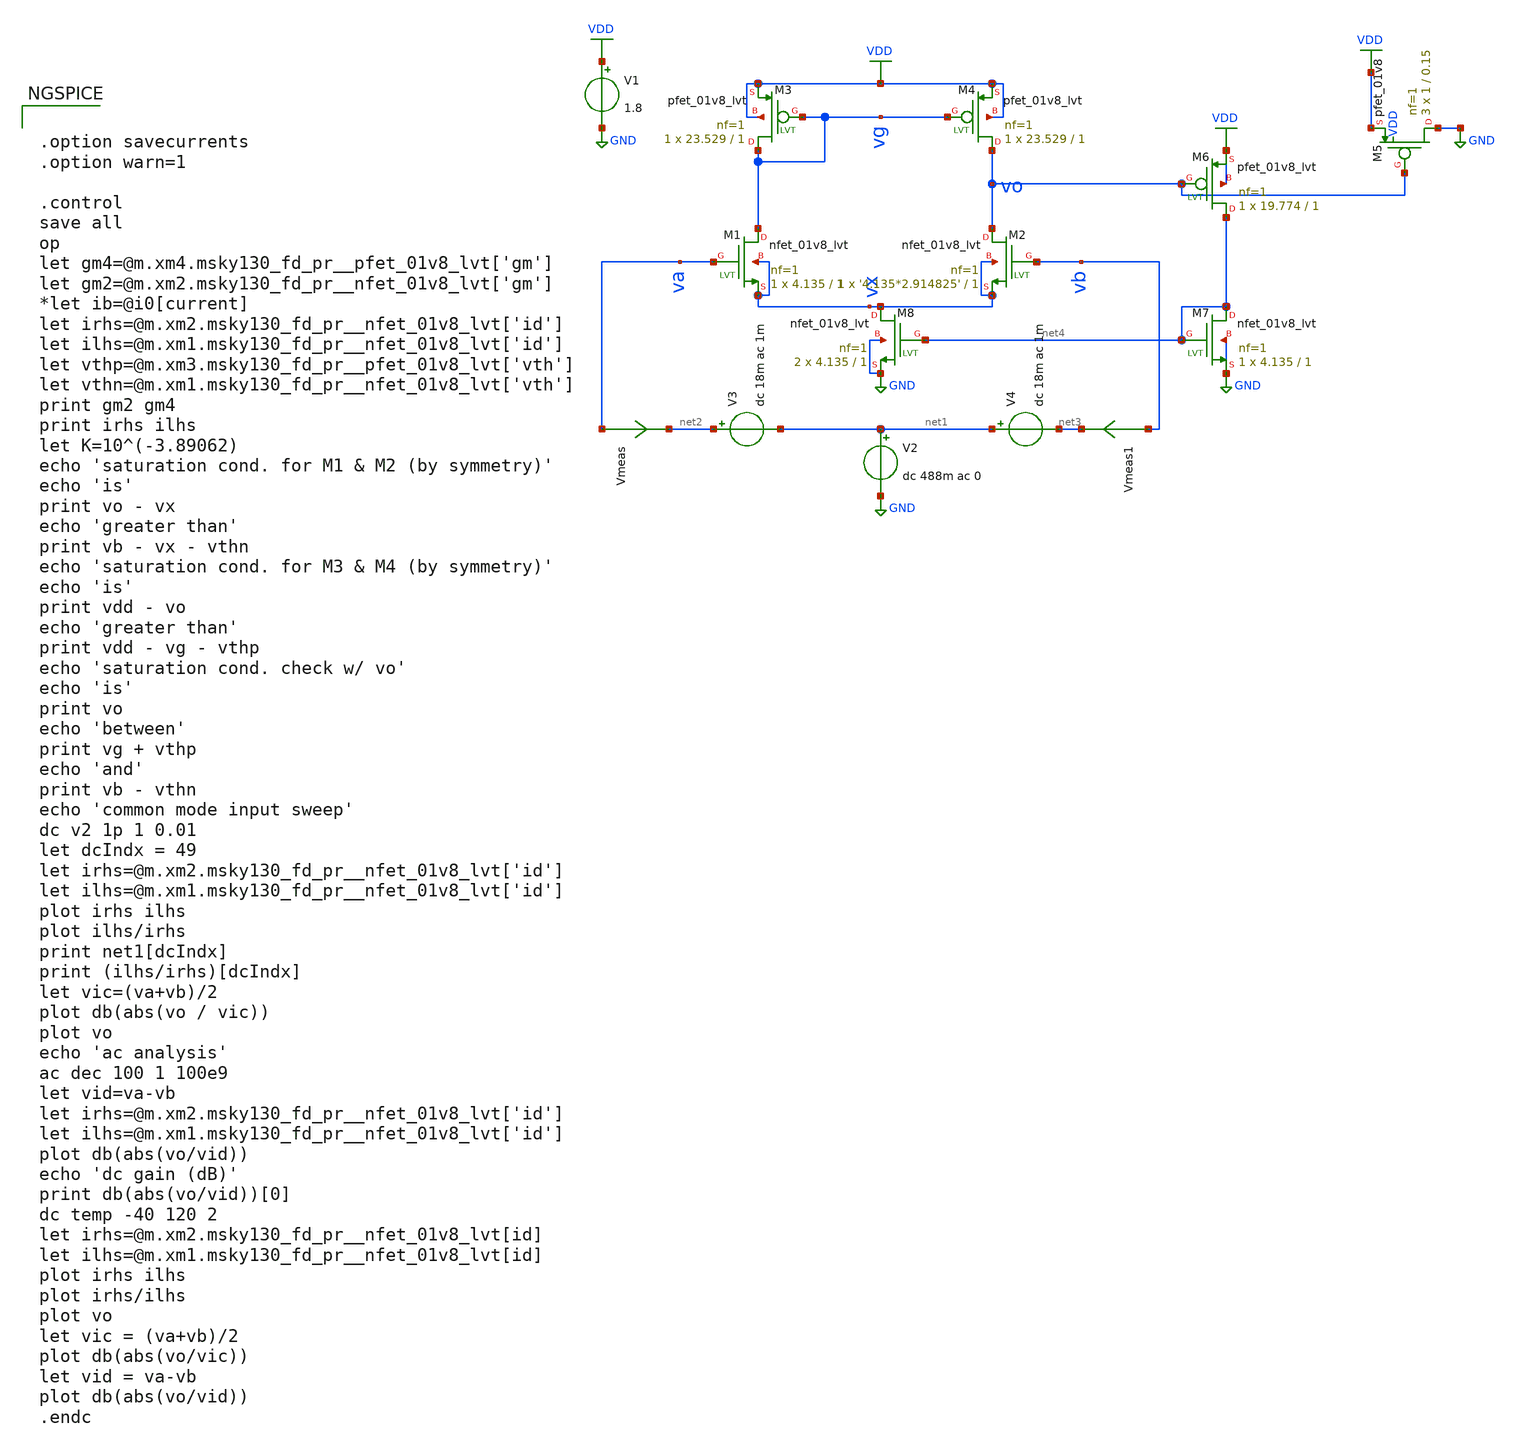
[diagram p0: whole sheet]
** sch_path: schematics/amplifier_with_bias_current.sch
**.subckt amplifier_with_bias_current
V1 VDD GND 1.8
V2 net1 GND dc 488m ac 0
Vmeas va net2 0
.save i(vmeas)
Vmeas1 vb net3 0
.save i(vmeas1)
XM5 GND vo VDD VDD sky130_fd_pr__pfet_01v8 L=0.15 W=1 nf=1 ad='int((nf+1)/2) * W/nf * 0.29' as='int((nf+2)/2) * W/nf * 0.29'
+ pd='2*int((nf+1)/2) * (W/nf + 0.29)' ps='2*int((nf+2)/2) * (W/nf + 0.29)' nrd='0.29 / W' nrs='0.29 / W'
+ sa=0 sb=0 sd=0 mult=3 m=3
V3 net2 net1 dc 18m ac 1m
V4 net1 net3 dc 18m ac 1m
XM4 vo vg VDD VDD sky130_fd_pr__pfet_01v8_lvt L=1 W=23.529 nf=1 ad='int((nf+1)/2) * W/nf * 0.29' as='int((nf+2)/2) * W/nf * 0.29'
+ pd='2*int((nf+1)/2) * (W/nf + 0.29)' ps='2*int((nf+2)/2) * (W/nf + 0.29)' nrd='0.29 / W' nrs='0.29 / W'
+ sa=0 sb=0 sd=0 mult=1 m=1
XM2 vo vb vx vx sky130_fd_pr__nfet_01v8_lvt L=1 W='4.135*2.914825' nf=1 ad='int((nf+1)/2) * W/nf * 0.29'
+ as='int((nf+2)/2) * W/nf * 0.29' pd='2*int((nf+1)/2) * (W/nf + 0.29)' ps='2*int((nf+2)/2) * (W/nf + 0.29)'
+ nrd='0.29 / W' nrs='0.29 / W' sa=0 sb=0 sd=0 mult=1 m=1
XM6 net4 vo VDD VDD sky130_fd_pr__pfet_01v8_lvt L=1 W=19.774 nf=1 ad='int((nf+1)/2) * W/nf * 0.29' as='int((nf+2)/2) * W/nf * 0.29'
+ pd='2*int((nf+1)/2) * (W/nf + 0.29)' ps='2*int((nf+2)/2) * (W/nf + 0.29)' nrd='0.29 / W' nrs='0.29 / W'
+ sa=0 sb=0 sd=0 mult=1 m=1
XM1 vg va vx vx sky130_fd_pr__nfet_01v8_lvt L=1 W=4.135 nf=1 ad='int((nf+1)/2) * W/nf * 0.29' as='int((nf+2)/2) * W/nf * 0.29'
+ pd='2*int((nf+1)/2) * (W/nf + 0.29)' ps='2*int((nf+2)/2) * (W/nf + 0.29)' nrd='0.29 / W' nrs='0.29 / W'
+ sa=0 sb=0 sd=0 mult=1 m=1
XM7 net4 net4 GND GND sky130_fd_pr__nfet_01v8_lvt L=1 W=4.135 nf=1 ad='int((nf+1)/2) * W/nf * 0.29' as='int((nf+2)/2) * W/nf * 0.29'
+ pd='2*int((nf+1)/2) * (W/nf + 0.29)' ps='2*int((nf+2)/2) * (W/nf + 0.29)' nrd='0.29 / W' nrs='0.29 / W'
+ sa=0 sb=0 sd=0 mult=1 m=1
XM3 vg vg VDD VDD sky130_fd_pr__pfet_01v8_lvt L=1 W=23.529 nf=1 ad='int((nf+1)/2) * W/nf * 0.29' as='int((nf+2)/2) * W/nf * 0.29'
+ pd='2*int((nf+1)/2) * (W/nf + 0.29)' ps='2*int((nf+2)/2) * (W/nf + 0.29)' nrd='0.29 / W' nrs='0.29 / W'
+ sa=0 sb=0 sd=0 mult=1 m=1
XM8 vx net4 GND GND sky130_fd_pr__nfet_01v8_lvt L=1 W=4.135 nf=1 ad='int((nf+1)/2) * W/nf * 0.29' as='int((nf+2)/2) * W/nf * 0.29'
+ pd='2*int((nf+1)/2) * (W/nf + 0.29)' ps='2*int((nf+2)/2) * (W/nf + 0.29)' nrd='0.29 / W' nrs='0.29 / W'
+ sa=0 sb=0 sd=0 mult=2 m=2
**** begin user architecture code


.option savecurrents
.option warn=1

.control
save all
op
let gm4=@m.xm4.msky130_fd_pr__pfet_01v8_lvt['gm']
let gm2=@m.xm2.msky130_fd_pr__nfet_01v8_lvt['gm']
*let ib=@i0[current]
let irhs=@m.xm2.msky130_fd_pr__nfet_01v8_lvt['id']
let ilhs=@m.xm1.msky130_fd_pr__nfet_01v8_lvt['id']
let vthp=@m.xm3.msky130_fd_pr__pfet_01v8_lvt['vth']
let vthn=@m.xm1.msky130_fd_pr__nfet_01v8_lvt['vth']
print gm2 gm4
print irhs ilhs
let K=10^(-3.89062)
echo 'saturation cond. for M1 & M2 (by symmetry)'
echo 'is'
print vo - vx
echo 'greater than'
print vb - vx - vthn
echo 'saturation cond. for M3 & M4 (by symmetry)'
echo 'is'
print vdd - vo
echo 'greater than'
print vdd - vg - vthp
echo 'saturation cond. check w/ vo'
echo 'is'
print vo
echo 'between'
print vg + vthp
echo 'and'
print vb - vthn
echo 'common mode input sweep'
dc v2 1p 1 0.01
let dcIndx = 49
let irhs=@m.xm2.msky130_fd_pr__nfet_01v8_lvt['id']
let ilhs=@m.xm1.msky130_fd_pr__nfet_01v8_lvt['id']
plot irhs ilhs
plot ilhs/irhs
print net1[dcIndx]
print (ilhs/irhs)[dcIndx]
let vic=(va+vb)/2
plot db(abs(vo / vic))
plot vo
echo 'ac analysis'
ac dec 100 1 100e9
let vid=va-vb
let irhs=@m.xm2.msky130_fd_pr__nfet_01v8_lvt['id']
let ilhs=@m.xm1.msky130_fd_pr__nfet_01v8_lvt['id']
plot db(abs(vo/vid))
echo 'dc gain (dB)'
print db(abs(vo/vid))[0]
dc temp -40 120 2
let irhs=@m.xm2.msky130_fd_pr__nfet_01v8_lvt[id]
let ilhs=@m.xm1.msky130_fd_pr__nfet_01v8_lvt[id]
plot irhs ilhs
plot irhs/ilhs
plot vo
let vic = (va+vb)/2
plot db(abs(vo/vic))
let vid = va-vb
plot db(abs(vo/vid))
.endc



.include $::SKYWATER_MODELS/cells/nfet_01v8/sky130_fd_pr__nfet_01v8__tt.corner.spice
.include $::SKYWATER_MODELS/cells/nfet_01v8_lvt/sky130_fd_pr__nfet_01v8_lvt__tt.corner.spice
.include $::SKYWATER_MODELS/cells/pfet_01v8/sky130_fd_pr__pfet_01v8__tt.corner.spice
.include $::SKYWATER_MODELS/cells/nfet_03v3_nvt/sky130_fd_pr__nfet_03v3_nvt__tt.corner.spice
.include $::SKYWATER_MODELS/cells/nfet_05v0_nvt/sky130_fd_pr__nfet_05v0_nvt__tt.corner.spice
.include $::SKYWATER_MODELS/cells/esd_nfet_01v8/sky130_fd_pr__esd_nfet_01v8__tt.corner.spice
.include $::SKYWATER_MODELS/cells/pfet_01v8_lvt/sky130_fd_pr__pfet_01v8_lvt__tt.corner.spice
.include $::SKYWATER_MODELS/cells/pfet_01v8_hvt/sky130_fd_pr__pfet_01v8_hvt__tt.corner.spice
.include $::SKYWATER_MODELS/cells/esd_pfet_g5v0d10v5/sky130_fd_pr__esd_pfet_g5v0d10v5__tt.corner.spice
.include $::SKYWATER_MODELS/cells/pfet_g5v0d10v5/sky130_fd_pr__pfet_g5v0d10v5__tt.corner.spice
.include $::SKYWATER_MODELS/cells/pfet_g5v0d16v0/sky130_fd_pr__pfet_g5v0d16v0__tt.corner.spice
.include $::SKYWATER_MODELS/cells/nfet_g5v0d10v5/sky130_fd_pr__nfet_g5v0d10v5__tt.corner.spice
.include $::SKYWATER_MODELS/cells/nfet_g5v0d16v0/sky130_fd_pr__nfet_g5v0d16v0__tt_discrete.corner.spice
.include $::SKYWATER_MODELS/cells/esd_nfet_g5v0d10v5/sky130_fd_pr__esd_nfet_g5v0d10v5__tt.corner.spice
.include $::SKYWATER_MODELS/models/corners/tt/nonfet.spice
* Mismatch parameters
.include $::SKYWATER_MODELS/cells/nfet_01v8/sky130_fd_pr__nfet_01v8__mismatch.corner.spice
.include $::SKYWATER_MODELS/cells/pfet_01v8/sky130_fd_pr__pfet_01v8__mismatch.corner.spice
.include $::SKYWATER_MODELS/cells/nfet_01v8_lvt/sky130_fd_pr__nfet_01v8_lvt__mismatch.corner.spice
.include $::SKYWATER_MODELS/cells/pfet_01v8_lvt/sky130_fd_pr__pfet_01v8_lvt__mismatch.corner.spice
.include $::SKYWATER_MODELS/cells/pfet_01v8_hvt/sky130_fd_pr__pfet_01v8_hvt__mismatch.corner.spice
.include $::SKYWATER_MODELS/cells/nfet_g5v0d10v5/sky130_fd_pr__nfet_g5v0d10v5__mismatch.corner.spice
.include $::SKYWATER_MODELS/cells/pfet_g5v0d10v5/sky130_fd_pr__pfet_g5v0d10v5__mismatch.corner.spice
.include $::SKYWATER_MODELS/cells/nfet_05v0_nvt/sky130_fd_pr__nfet_05v0_nvt__mismatch.corner.spice
.include $::SKYWATER_MODELS/cells/nfet_03v3_nvt/sky130_fd_pr__nfet_03v3_nvt__mismatch.corner.spice
* Resistor$::SKYWATER_MODELS/Capacitor
.include $::SKYWATER_MODELS/models/r+c/res_typical__cap_typical.spice
.include $::SKYWATER_MODELS/models/r+c/res_typical__cap_typical__lin.spice
* Special cells
.include $::SKYWATER_MODELS/models/corners/tt/specialized_cells.spice
* All models
.include $::SKYWATER_MODELS/models/all.spice
.include $::SKYWATER_MODELS/cells/pnp_05v5/sky130_fd_pr__pnp_05v5_W3p40L3p40.model.spice
* Corner
.include $::SKYWATER_MODELS/models/corners/tt/rf.spice

**** end user architecture code
**.ends
.GLOBAL GND
.GLOBAL VDD
.end
